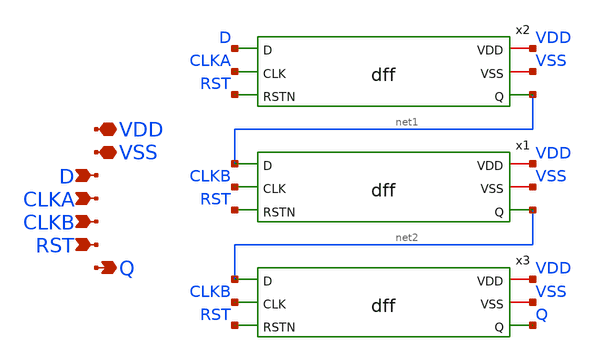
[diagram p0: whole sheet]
** sch_path: designs/libs/core_analog/switch-matrix/dff2clk.sch
**.subckt dff2clk VDD VSS D CLKA Q CLKB RST
*.iopin VDD
*.iopin VSS
*.ipin D
*.ipin CLKA
*.opin Q
*.ipin CLKB
*.ipin RST
x2 VDD VSS D CLKA RST net1 dff
x1 VDD VSS net1 CLKB RST net2 dff
x3 VDD VSS net2 CLKB RST Q dff
**.ends

* expanding   symbol:  dff.sym # of pins=6
** sym_path: designs/libs/core_analog/switch-matrix/dff.sym
** sch_path: designs/libs/core_analog/switch-matrix/dff.sch
.subckt dff VDD VSS D CLK RSTN Q
*.iopin VDD
*.iopin VSS
*.ipin D
*.ipin CLK
*.opin Q
*.ipin RSTN
x1 VDD VSS net1 net4 net2 nand2_1
x3 VDD VSS net4 QN Q nand2_1
x4 VDD VSS Q net3 RSTN QN nand3_1
x6 VDD VSS net2 CLK RSTN net4 nand3_1
x2 VDD VSS net4 CLK net1 net3 nand3_1
x7 VDD VSS net3 D RSTN net1 nand3_1
.ends


* expanding   symbol:  nand2_1.sym # of pins=5
** sym_path: designs/libs/core_analog/switch-matrix/nand2_1.sym
** sch_path: designs/libs/core_analog/switch-matrix/nand2_1.sch
.subckt nand2_1 VDD VSS A B Y
*.iopin VDD
*.iopin VSS
*.ipin A
*.ipin B
*.opin Y
XM2 Y A VDD VDD pfet_03v3 L=0.3u W=1.5u nf=1 ad='int((nf+1)/2) * W/nf * 0.18u' as='int((nf+2)/2) * W/nf * 0.18u'
+ pd='2*int((nf+1)/2) * (W/nf + 0.18u)' ps='2*int((nf+2)/2) * (W/nf + 0.18u)' nrd='0.18u / W' nrs='0.18u / W'
+ sa=0 sb=0 sd=0 m=1
XM1 Y B VDD VDD pfet_03v3 L=0.3u W=1.5u nf=1 ad='int((nf+1)/2) * W/nf * 0.18u' as='int((nf+2)/2) * W/nf * 0.18u'
+ pd='2*int((nf+1)/2) * (W/nf + 0.18u)' ps='2*int((nf+2)/2) * (W/nf + 0.18u)' nrd='0.18u / W' nrs='0.18u / W'
+ sa=0 sb=0 sd=0 m=1
XM4 Y A net1 VSS nfet_03v3 L=0.3u W=0.5u nf=1 ad='int((nf+1)/2) * W/nf * 0.18u' as='int((nf+2)/2) * W/nf * 0.18u'
+ pd='2*int((nf+1)/2) * (W/nf + 0.18u)' ps='2*int((nf+2)/2) * (W/nf + 0.18u)' nrd='0.18u / W' nrs='0.18u / W'
+ sa=0 sb=0 sd=0 m=1
XM3 net1 B VSS VSS nfet_03v3 L=0.3u W=0.5u nf=1 ad='int((nf+1)/2) * W/nf * 0.18u' as='int((nf+2)/2) * W/nf * 0.18u'
+ pd='2*int((nf+1)/2) * (W/nf + 0.18u)' ps='2*int((nf+2)/2) * (W/nf + 0.18u)' nrd='0.18u / W' nrs='0.18u / W'
+ sa=0 sb=0 sd=0 m=1
.ends


* expanding   symbol:  nand3_1.sym # of pins=6
** sym_path: designs/libs/core_analog/switch-matrix/nand3_1.sym
** sch_path: designs/libs/core_analog/switch-matrix/nand3_1.sch
.subckt nand3_1 VDD VSS A B C Y
*.iopin VDD
*.iopin VSS
*.ipin A
*.ipin B
*.opin Y
*.ipin C
XM2 Y A VDD VDD pfet_03v3 L=0.3u W=1.5u nf=1 ad='int((nf+1)/2) * W/nf * 0.18u' as='int((nf+2)/2) * W/nf * 0.18u'
+ pd='2*int((nf+1)/2) * (W/nf + 0.18u)' ps='2*int((nf+2)/2) * (W/nf + 0.18u)' nrd='0.18u / W' nrs='0.18u / W'
+ sa=0 sb=0 sd=0 m=1
XM1 Y B VDD VDD pfet_03v3 L=0.3u W=1.5u nf=1 ad='int((nf+1)/2) * W/nf * 0.18u' as='int((nf+2)/2) * W/nf * 0.18u'
+ pd='2*int((nf+1)/2) * (W/nf + 0.18u)' ps='2*int((nf+2)/2) * (W/nf + 0.18u)' nrd='0.18u / W' nrs='0.18u / W'
+ sa=0 sb=0 sd=0 m=1
XM6 Y C VDD VDD pfet_03v3 L=0.3u W=1.5u nf=1 ad='int((nf+1)/2) * W/nf * 0.18u' as='int((nf+2)/2) * W/nf * 0.18u'
+ pd='2*int((nf+1)/2) * (W/nf + 0.18u)' ps='2*int((nf+2)/2) * (W/nf + 0.18u)' nrd='0.18u / W' nrs='0.18u / W'
+ sa=0 sb=0 sd=0 m=1
XM4 Y A net2 VSS nfet_03v3 L=0.3u W=0.5u nf=1 ad='int((nf+1)/2) * W/nf * 0.18u' as='int((nf+2)/2) * W/nf * 0.18u'
+ pd='2*int((nf+1)/2) * (W/nf + 0.18u)' ps='2*int((nf+2)/2) * (W/nf + 0.18u)' nrd='0.18u / W' nrs='0.18u / W'
+ sa=0 sb=0 sd=0 m=1
XM3 net2 B net1 VSS nfet_03v3 L=0.3u W=0.5u nf=1 ad='int((nf+1)/2) * W/nf * 0.18u' as='int((nf+2)/2) * W/nf * 0.18u'
+ pd='2*int((nf+1)/2) * (W/nf + 0.18u)' ps='2*int((nf+2)/2) * (W/nf + 0.18u)' nrd='0.18u / W' nrs='0.18u / W'
+ sa=0 sb=0 sd=0 m=1
XM5 net1 C VSS VSS nfet_03v3 L=0.3u W=0.5u nf=1 ad='int((nf+1)/2) * W/nf * 0.18u' as='int((nf+2)/2) * W/nf * 0.18u'
+ pd='2*int((nf+1)/2) * (W/nf + 0.18u)' ps='2*int((nf+2)/2) * (W/nf + 0.18u)' nrd='0.18u / W' nrs='0.18u / W'
+ sa=0 sb=0 sd=0 m=1
.ends

.end
